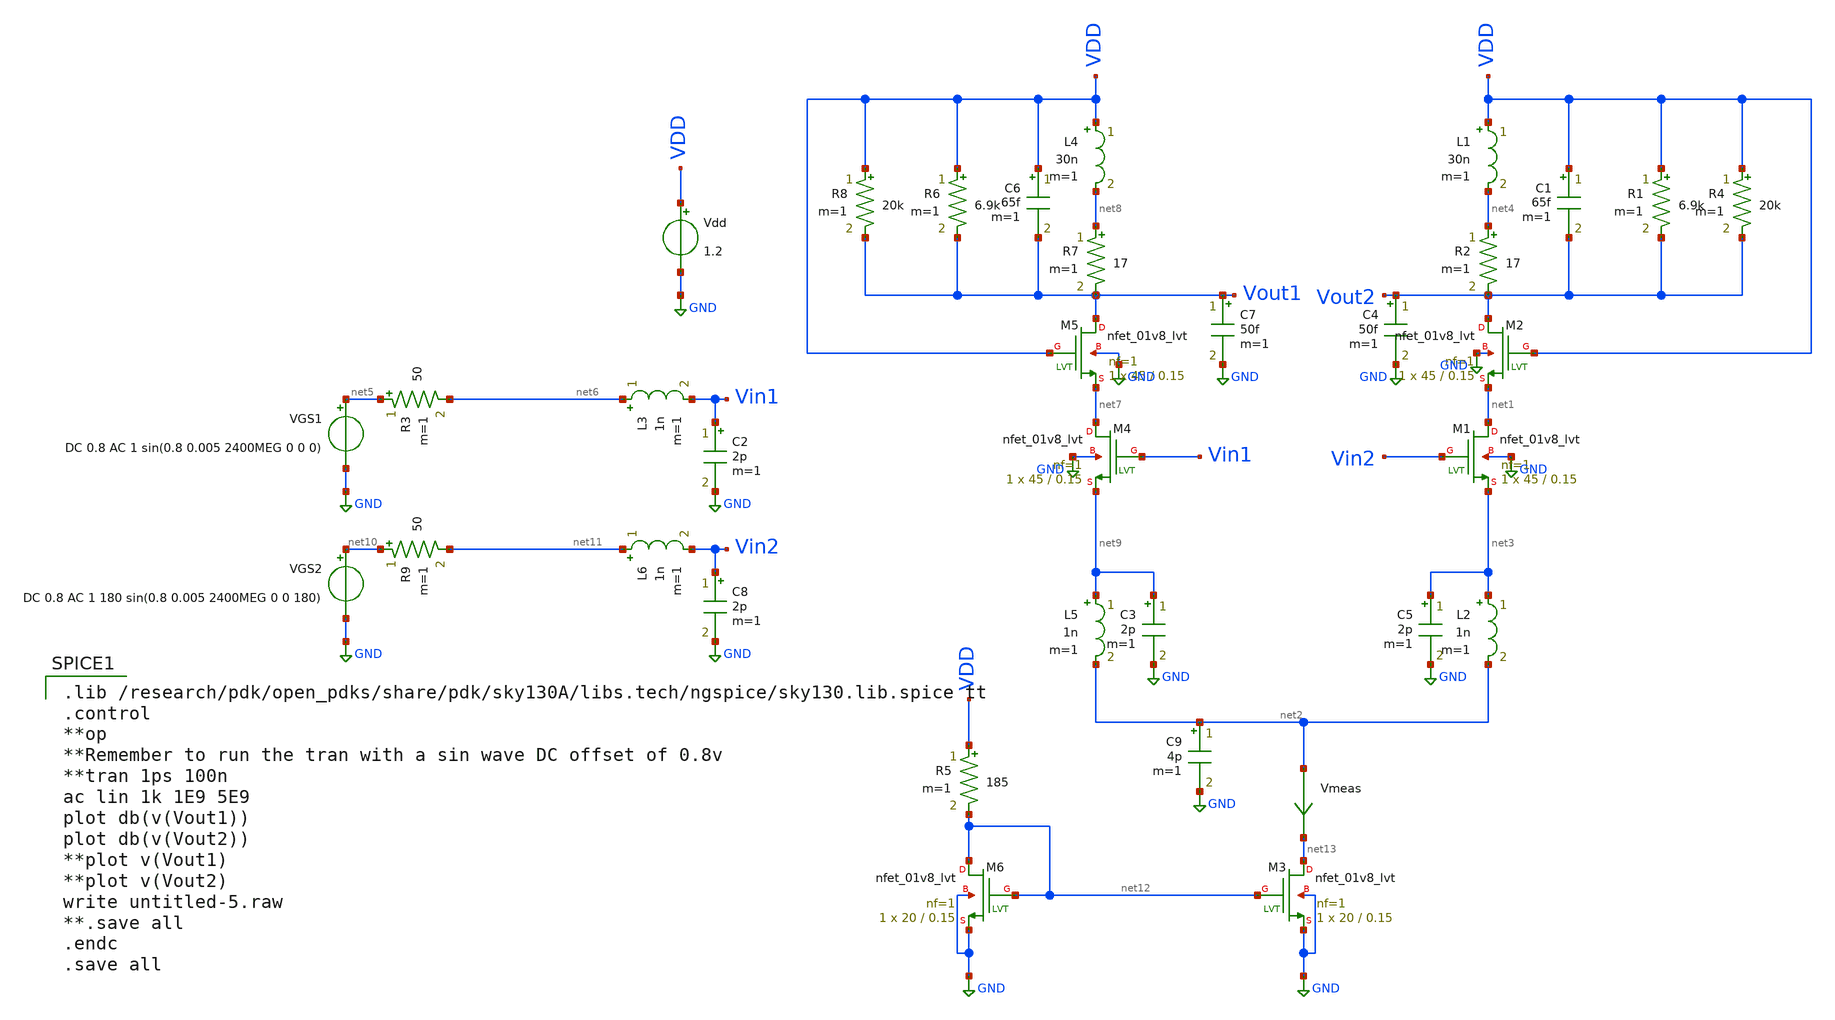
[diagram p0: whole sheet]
** sch_path: skywater_stuff/ECE631_RF_CMOS/Diff_LNA.sch
**.subckt Diff_LNA
XM1 net1 Vin2 net3 GND sky130_fd_pr__nfet_01v8_lvt L=0.15 W=45 nf=1 ad='int((nf+1)/2) * W/nf * 0.29'
+ as='int((nf+2)/2) * W/nf * 0.29' pd='2*int((nf+1)/2) * (W/nf + 0.29)' ps='2*int((nf+2)/2) * (W/nf + 0.29)'
+ nrd='0.29 / W' nrs='0.29 / W' sa=0 sb=0 sd=0 mult=1 m=1
L1 VDD net4 30n m=1
Vdd VDD GND 1.2
XM2 Vout2 VDD net1 GND sky130_fd_pr__nfet_01v8_lvt L=0.15 W=45 nf=1 ad='int((nf+1)/2) * W/nf * 0.29'
+ as='int((nf+2)/2) * W/nf * 0.29' pd='2*int((nf+1)/2) * (W/nf + 0.29)' ps='2*int((nf+2)/2) * (W/nf + 0.29)'
+ nrd='0.29 / W' nrs='0.29 / W' sa=0 sb=0 sd=0 mult=1 m=1
VGS1 net5 GND DC 0.8 AC 1 sin(0.8 0.005 2400MEG 0 0 0)
C1 VDD Vout2 65f m=1
L2 net3 net2 1n m=1
R1 VDD Vout2 6.9k m=1
R2 net4 Vout2 17 m=1
R3 net5 net6 50 m=1
C2 Vin1 GND 2p m=1
L3 net6 Vin1 1n m=1
C4 Vout2 GND 50f m=1
R4 VDD Vout2 20k m=1
XM4 net7 Vin1 net9 GND sky130_fd_pr__nfet_01v8_lvt L=0.15 W=45 nf=1 ad='int((nf+1)/2) * W/nf * 0.29'
+ as='int((nf+2)/2) * W/nf * 0.29' pd='2*int((nf+1)/2) * (W/nf + 0.29)' ps='2*int((nf+2)/2) * (W/nf + 0.29)'
+ nrd='0.29 / W' nrs='0.29 / W' sa=0 sb=0 sd=0 mult=1 m=1
L4 VDD net8 30n m=1
XM5 Vout1 VDD net7 GND sky130_fd_pr__nfet_01v8_lvt L=0.15 W=45 nf=1 ad='int((nf+1)/2) * W/nf * 0.29'
+ as='int((nf+2)/2) * W/nf * 0.29' pd='2*int((nf+1)/2) * (W/nf + 0.29)' ps='2*int((nf+2)/2) * (W/nf + 0.29)'
+ nrd='0.29 / W' nrs='0.29 / W' sa=0 sb=0 sd=0 mult=1 m=1
C6 VDD Vout1 65f m=1
R6 VDD Vout1 6.9k m=1
R7 net8 Vout1 17 m=1
C7 Vout1 GND 50f m=1
R8 VDD Vout1 20k m=1
L5 net9 net2 1n m=1
VGS2 net10 GND DC 0.8 AC 1 180 sin(0.8 0.005 2400MEG 0 0 180)
R9 net10 net11 50 m=1
C8 Vin2 GND 2p m=1
L6 net11 Vin2 1n m=1
XM3 net13 net12 GND GND sky130_fd_pr__nfet_01v8_lvt L=0.15 W=20 nf=1 ad='int((nf+1)/2) * W/nf * 0.29'
+ as='int((nf+2)/2) * W/nf * 0.29' pd='2*int((nf+1)/2) * (W/nf + 0.29)' ps='2*int((nf+2)/2) * (W/nf + 0.29)'
+ nrd='0.29 / W' nrs='0.29 / W' sa=0 sb=0 sd=0 mult=1 m=1
XM6 net12 net12 GND GND sky130_fd_pr__nfet_01v8_lvt L=0.15 W=20 nf=1 ad='int((nf+1)/2) * W/nf * 0.29'
+ as='int((nf+2)/2) * W/nf * 0.29' pd='2*int((nf+1)/2) * (W/nf + 0.29)' ps='2*int((nf+2)/2) * (W/nf + 0.29)'
+ nrd='0.29 / W' nrs='0.29 / W' sa=0 sb=0 sd=0 mult=1 m=1
R5 VDD net12 185 m=1
Vmeas net2 net13 0
.save i(vmeas)
C3 net9 GND 2p m=1
C5 net3 GND 2p m=1
C9 net2 GND 4p m=1
**** begin user architecture code

.lib /research/pdk/open_pdks/share/pdk/sky130A/libs.tech/ngspice/sky130.lib.spice tt
.control
**op
**Remember to run the tran with a sin wave DC offset of 0.8v
**tran 1ps 100n
ac lin 1k 1E9 5E9
plot db(v(Vout1))
plot db(v(Vout2))
**plot v(Vout1)
**plot v(Vout2)
write untitled-5.raw
**.save all
.endc
.save all


**** end user architecture code
**.ends
.GLOBAL GND
.end
